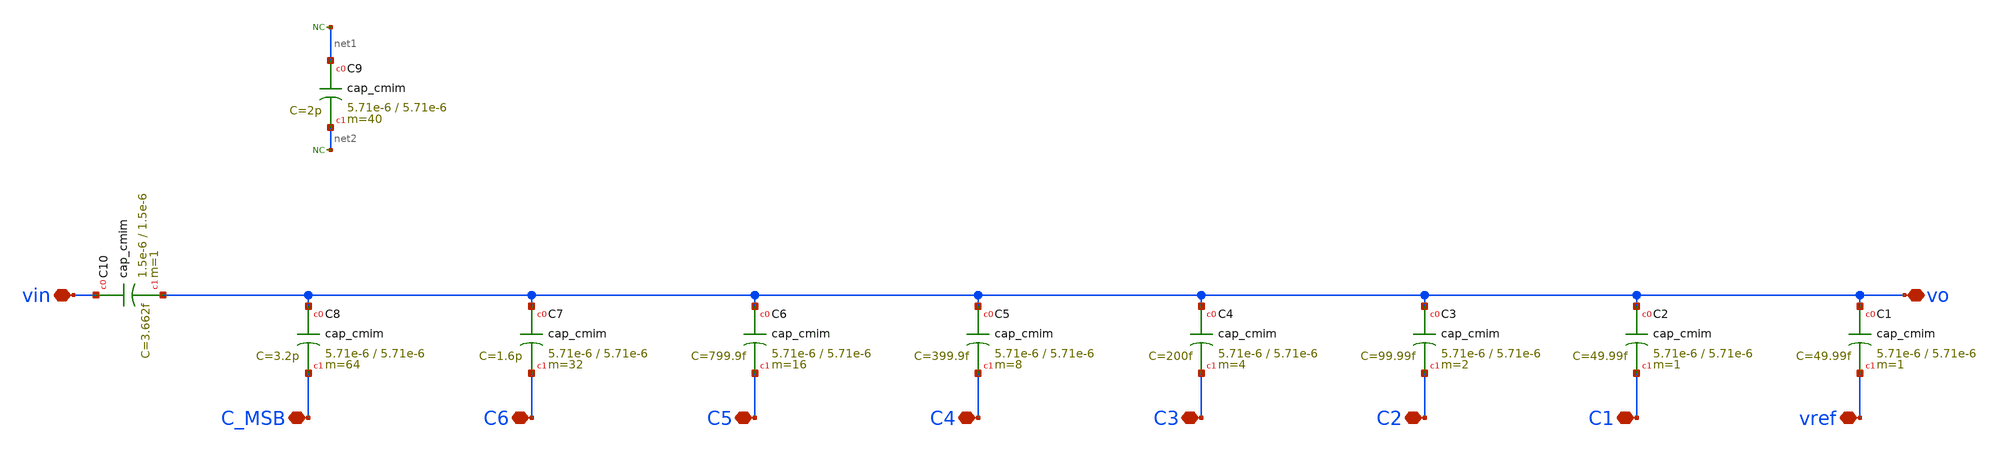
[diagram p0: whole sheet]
** sch_path: dependencies/ADC/dependencies/SAR_ADC_8BIT_IHP/xschem/CDAC.sch
**.subckt CDAC vin vo C6 C5 C4 C3 C2 C1 vref C_MSB
*.iopin vin
*.iopin vo
*.iopin C6
*.iopin C5
*.iopin C4
*.iopin C3
*.iopin C2
*.iopin C1
*.iopin vref
*.iopin C_MSB
XC1 vo vref cap_cmim w=5.71e-6 l=5.71e-6 m=1 mm_ok=1
XC2 vo C1 cap_cmim w=5.71e-6 l=5.71e-6 m=1 mm_ok=1
XC3 vo C2 cap_cmim w=5.71e-6 l=5.71e-6 m=2 mm_ok=1
XC4 vo C3 cap_cmim w=5.71e-6 l=5.71e-6 m=4 mm_ok=1
XC5 vo C4 cap_cmim w=5.71e-6 l=5.71e-6 m=8 mm_ok=1
XC6 vo C5 cap_cmim w=5.71e-6 l=5.71e-6 m=16 mm_ok=1
XC7 vo C6 cap_cmim w=5.71e-6 l=5.71e-6 m=32 mm_ok=1
XC8 vo C_MSB cap_cmim w=5.71e-6 l=5.71e-6 m=64 mm_ok=1
XC9 net1 net2 cap_cmim w=5.71e-6 l=5.71e-6 m=40 mm_ok=1
* noconn #net1
* noconn #net2
XC10 vin vo cap_cmim w=1.5e-6 l=1.5e-6 m=1 mm_ok=1
**.ends
.end
